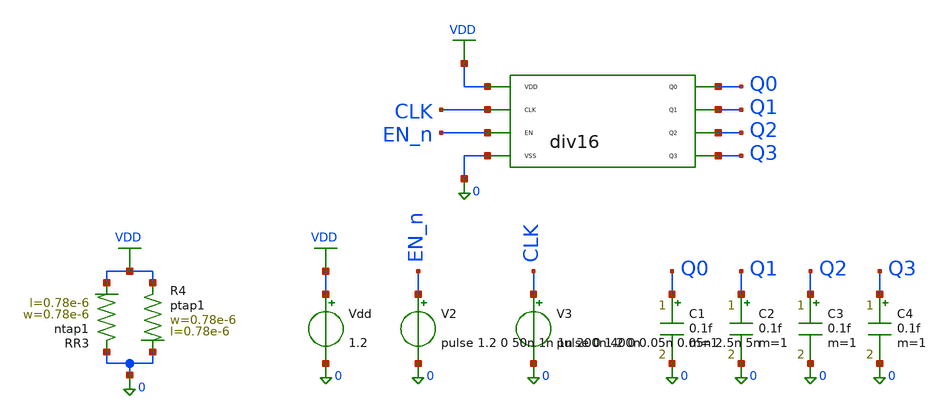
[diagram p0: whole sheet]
** sch_path: TSENSE8490-main/schematic/xschem/digital/div16/xschem/div16-tb.sch
**.subckt div16-tb
Vdd VDD 0 1.2
XR3 0 VDD ntap1 R=262.8 w=0.78e-6 l=0.78e-6
XR4 VDD 0 ptap1 R=262.8 w=0.78e-6 l=0.78e-6
V2 EN_n 0 pulse 1.2 0 50n 1n 1n 200n 400n
x1 0 VDD CLK EN_n Q0 Q1 Q2 Q3 div16
C1 Q0 0 0.1f m=1
C2 Q1 0 0.1f m=1
C3 Q2 0 0.1f m=1
C4 Q3 0 0.1f m=1
V3 CLK 0 pulse 0 1.2 0 0.05n 0.05n 2.5n 5n
**** begin user architecture code



** ngr_lib cornerMOSlv.lib mos_tt mos_ff mos_ss mos_tt_mismatch
** ngr_lib cornerRES.lib res_typ
** ngr_out f
** ngr_name div16-tb

.option rshunt=1e12
.option klu
*.param cpar=0
*.param lstarv=0.18u
.control
set rawfile = div16-tb.raw

tran 0.05n 1u

*meas tran tperiod
*  + TRIG v(ro_raw) VAL=0.6 RISE=2 TD=75n
*  + TARG v(ro_raw) VAL=0.6 RISE=3 TD=75n

write $rawfile clk en_n q0 q1 q2 q3
.endc






.lib cornerMOSlv.lib mos_tt
.lib cornerMOShv.lib mos_tt
.lib cornerRES.lib res_typ
.lib cornerDIO.lib dio_tt






.include sg13cmos5l_stdcell.spice
*.include digital/div16/div16.spice



**** end user architecture code
**.ends

* expanding   symbol:  digital/div16/xschem/div16.sym # of pins=8
** sym_path: TSENSE8490-main/schematic/xschem/lvs-view/digital/div16/xschem/div16.sym

* NGSPICE file created from div16.ext - technology: ihp-sg13cmos5l

* Black-box entry subcircuit for sg13cmos5l_decap_8 abstract view
.subckt sg13cmos5l_decap_8 VDD VSS
.ends

* Black-box entry subcircuit for sg13cmos5l_fill_2 abstract view
.subckt sg13cmos5l_fill_2 VDD VSS
.ends

* Black-box entry subcircuit for sg13cmos5l_fill_1 abstract view
.subckt sg13cmos5l_fill_1 VDD VSS
.ends

* Black-box entry subcircuit for sg13cmos5l_inv_1 abstract view
.subckt sg13cmos5l_inv_1 Y A VDD VSS
.ends

* Black-box entry subcircuit for sg13cmos5l_decap_4 abstract view
.subckt sg13cmos5l_decap_4 VDD VSS
.ends

* Black-box entry subcircuit for sg13cmos5l_buf_1 abstract view
.subckt sg13cmos5l_buf_1 X A VDD VSS
.ends

* Black-box entry subcircuit for sg13cmos5l_dfrbpq_1 abstract view
.subckt sg13cmos5l_dfrbpq_1 Q CLK D RESET_B VDD VSS
.ends

* Black-box entry subcircuit for sg13cmos5l_dlygate4sd3_1 abstract view
.subckt sg13cmos5l_dlygate4sd3_1 X A VDD VSS
.ends

.subckt div16 VDD VSS CLK EN Q0 Q1 Q2 Q3
XFILLER_0_35 VPWR VGND sg13cmos5l_decap_8
XFILLER_3_45 VPWR VGND sg13cmos5l_decap_8
XFILLER_0_14 VPWR VGND sg13cmos5l_decap_8
XFILLER_6_35 VPWR VGND sg13cmos5l_decap_8
XFILLER_6_46 VPWR VGND sg13cmos5l_fill_2
XFILLER_1_0 VPWR VGND sg13cmos5l_decap_8
XFILLER_3_59 VPWR VGND sg13cmos5l_fill_2
XFILLER_6_14 VPWR VGND sg13cmos5l_decap_8
XFILLER_0_28 VPWR VGND sg13cmos5l_decap_8
XFILLER_0_49 VPWR VGND sg13cmos5l_decap_8
XFILLER_3_38 VPWR VGND sg13cmos5l_decap_8
XFILLER_5_8 VPWR VGND sg13cmos5l_decap_8
XFILLER_6_59 VPWR VGND sg13cmos5l_fill_2
XFILLER_1_60 VPWR VGND sg13cmos5l_fill_1
XFILLER_6_28 VPWR VGND sg13cmos5l_decap_8
X_08_ _08_/Y _15_/A VPWR VGND sg13cmos5l_inv_1
X_09_ _09_/Y _15_/A VPWR VGND sg13cmos5l_inv_1
XFILLER_4_52 VPWR VGND sg13cmos5l_decap_4
XFILLER_1_21 VPWR VGND sg13cmos5l_decap_8
XFILLER_1_7 VPWR VGND sg13cmos5l_decap_8
XFILLER_4_45 VPWR VGND sg13cmos5l_decap_4
XFILLER_4_56 VPWR VGND sg13cmos5l_fill_1
XFILLER_6_0 VPWR VGND sg13cmos5l_decap_8
Xinput1 _15_/A meas_en VPWR VGND sg13cmos5l_buf_1
XFILLER_1_14 VPWR VGND sg13cmos5l_decap_8
XFILLER_1_58 VPWR VGND sg13cmos5l_fill_2
XFILLER_4_14 VPWR VGND sg13cmos5l_decap_4
XFILLER_4_0 VPWR VGND sg13cmos5l_decap_8
XFILLER_2_0 VPWR VGND sg13cmos5l_decap_8
XFILLER_2_52 VPWR VGND sg13cmos5l_decap_4
XFILLER_6_7 VPWR VGND sg13cmos5l_decap_8
XFILLER_2_42 VPWR VGND sg13cmos5l_fill_1
XFILLER_5_30 VPWR VGND sg13cmos5l_decap_4
XFILLER_0_0 VPWR VGND sg13cmos5l_decap_8
XFILLER_2_21 VPWR VGND sg13cmos5l_decap_8
XFILLER_4_7 VPWR VGND sg13cmos5l_decap_8
XFILLER_5_22 VPWR VGND sg13cmos5l_decap_4
X_19_ _19_/Q _18_/Q _19_/D _10_/Y VPWR VGND sg13cmos5l_dfrbpq_1
XFILLER_2_56 VPWR VGND sg13cmos5l_fill_1
X_18_ _18_/Q _17_/Q _18_/D _09_/Y VPWR VGND sg13cmos5l_dfrbpq_1
XFILLER_2_35 VPWR VGND sg13cmos5l_decap_8
X_17_ _17_/Q _16_/Q _17_/D _08_/Y VPWR VGND sg13cmos5l_dfrbpq_1
XFILLER_2_14 VPWR VGND sg13cmos5l_decap_8
XFILLER_2_7 VPWR VGND sg13cmos5l_decap_8
X_16_ _16_/Q clk_in _16_/D _15_/Y VPWR VGND sg13cmos5l_dfrbpq_1
Xhold6 _11_/A _16_/Q VPWR VGND sg13cmos5l_dlygate4sd3_1
XFILLER_5_15 VPWR VGND sg13cmos5l_decap_4
XFILLER_5_26 VPWR VGND sg13cmos5l_fill_1
X_15_ _15_/Y _15_/A VPWR VGND sg13cmos5l_inv_1
XFILLER_0_60 VPWR VGND sg13cmos5l_fill_1
XFILLER_0_7 VPWR VGND sg13cmos5l_decap_8
XFILLER_2_28 VPWR VGND sg13cmos5l_decap_4
X_14_ _19_/D _19_/Q VPWR VGND sg13cmos5l_inv_1
X_12_ _17_/D _17_/Q VPWR VGND sg13cmos5l_inv_1
X_13_ _18_/D _18_/Q VPWR VGND sg13cmos5l_inv_1
X_11_ _16_/D _11_/A VPWR VGND sg13cmos5l_inv_1
XFILLER_0_42 VPWR VGND sg13cmos5l_decap_8
XFILLER_3_52 VPWR VGND sg13cmos5l_decap_8
X_10_ _10_/Y _15_/A VPWR VGND sg13cmos5l_inv_1
Xoutput2 q0 _16_/Q VPWR VGND sg13cmos5l_buf_1
XFILLER_0_21 VPWR VGND sg13cmos5l_decap_8
XFILLER_6_52 VPWR VGND sg13cmos5l_decap_8
Xoutput3 q1 _17_/Q VPWR VGND sg13cmos5l_buf_1
XFILLER_6_21 VPWR VGND sg13cmos5l_decap_8
XFILLER_6_42 VPWR VGND sg13cmos5l_decap_4
Xoutput4 q2 _18_/Q VPWR VGND sg13cmos5l_buf_1
XFILLER_0_56 VPWR VGND sg13cmos5l_decap_4
XFILLER_3_0 VPWR VGND sg13cmos5l_fill_2
Xoutput5 q3 _19_/Q VPWR VGND sg13cmos5l_buf_1
.ends



.GLOBAL VDD
.end
